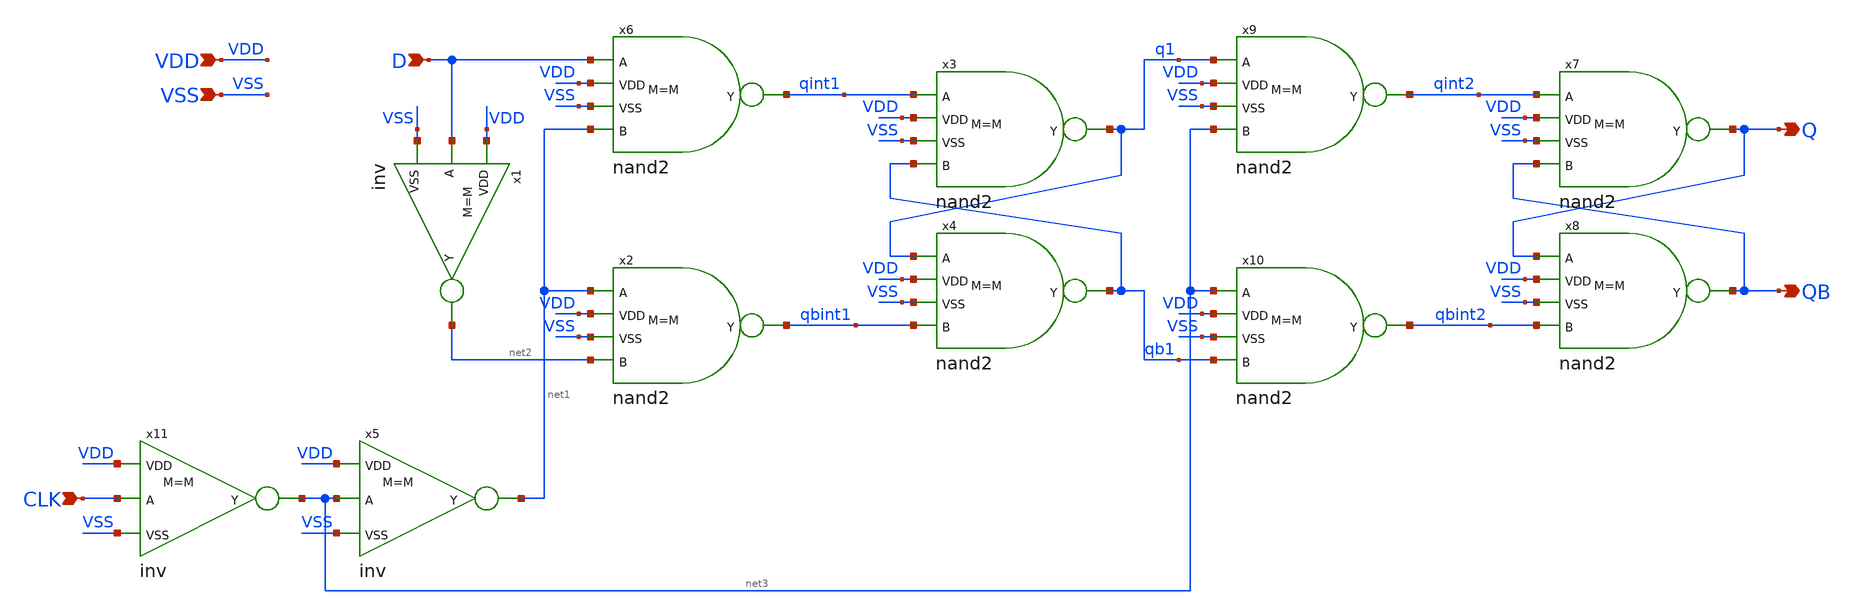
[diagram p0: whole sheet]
** sch_path: designs/dff.sch
**.subckt dff D CLK Q QB VDD VSS
*.ipin D
*.ipin CLK
*.opin Q
*.opin QB
*.ipin VDD
*.ipin VSS
x3 qint1 q1 qb1 VDD VSS nand2 M=M
x4 q1 qb1 qbint1 VDD VSS nand2 M=M
x6 D qint1 net1 VDD VSS nand2 M=M
x2 net1 qbint1 net2 VDD VSS nand2 M=M
x5 net3 net1 VDD VSS inv M=M
x1 D net2 VDD VSS inv M=M
x7 qint2 Q QB VDD VSS nand2 M=M
x8 Q QB qbint2 VDD VSS nand2 M=M
x9 q1 qint2 net3 VDD VSS nand2 M=M
x10 net3 qbint2 qb1 VDD VSS nand2 M=M
x11 CLK net3 VDD VSS inv M=M
**.ends
.end
